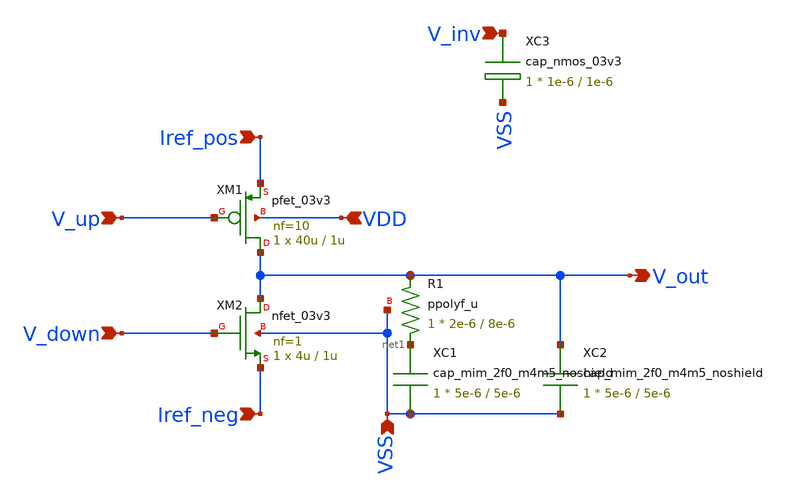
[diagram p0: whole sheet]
** sch_path: blocks/pll/cpump.sch
**.subckt cpump Iref_pos Iref_neg V_up V_down V_inv VDD VSS V_out
*.ipin Iref_pos
*.ipin Iref_neg
*.ipin V_up
*.ipin V_down
*.ipin V_inv
*.ipin VDD
*.ipin VSS
*.opin V_out
XM1 V_out V_up Iref_pos VDD pfet_03v3 L=1u W=40u nf=10 ad='int((nf+1)/2) * W/nf * 0.18u' as='int((nf+2)/2) * W/nf * 0.18u'
+ pd='2*int((nf+1)/2) * (W/nf + 0.18u)' ps='2*int((nf+2)/2) * (W/nf + 0.18u)' nrd='0.18u / W' nrs='0.18u / W'
+ sa=0 sb=0 sd=0 m=1
XM2 V_out V_down Iref_neg VSS nfet_03v3 L=1u W=4u nf=1 ad='int((nf+1)/2) * W/nf * 0.18u' as='int((nf+2)/2) * W/nf * 0.18u'
+ pd='2*int((nf+1)/2) * (W/nf + 0.18u)' ps='2*int((nf+2)/2) * (W/nf + 0.18u)' nrd='0.18u / W' nrs='0.18u / W'
+ sa=0 sb=0 sd=0 m=1
XR1 net1 V_out VSS ppolyf_u r_width=2e-6 r_length=8e-6 m=1
XC3 V_inv VSS cap_nmos_03v3 c_width=1e-6 c_length=1e-6 m=1
XC1 net1 VSS cap_mim_2f0_m4m5_noshield c_width=5e-6 c_length=5e-6 m=1
XC2 V_out VSS cap_mim_2f0_m4m5_noshield c_width=5e-6 c_length=5e-6 m=1
**.ends
.end
